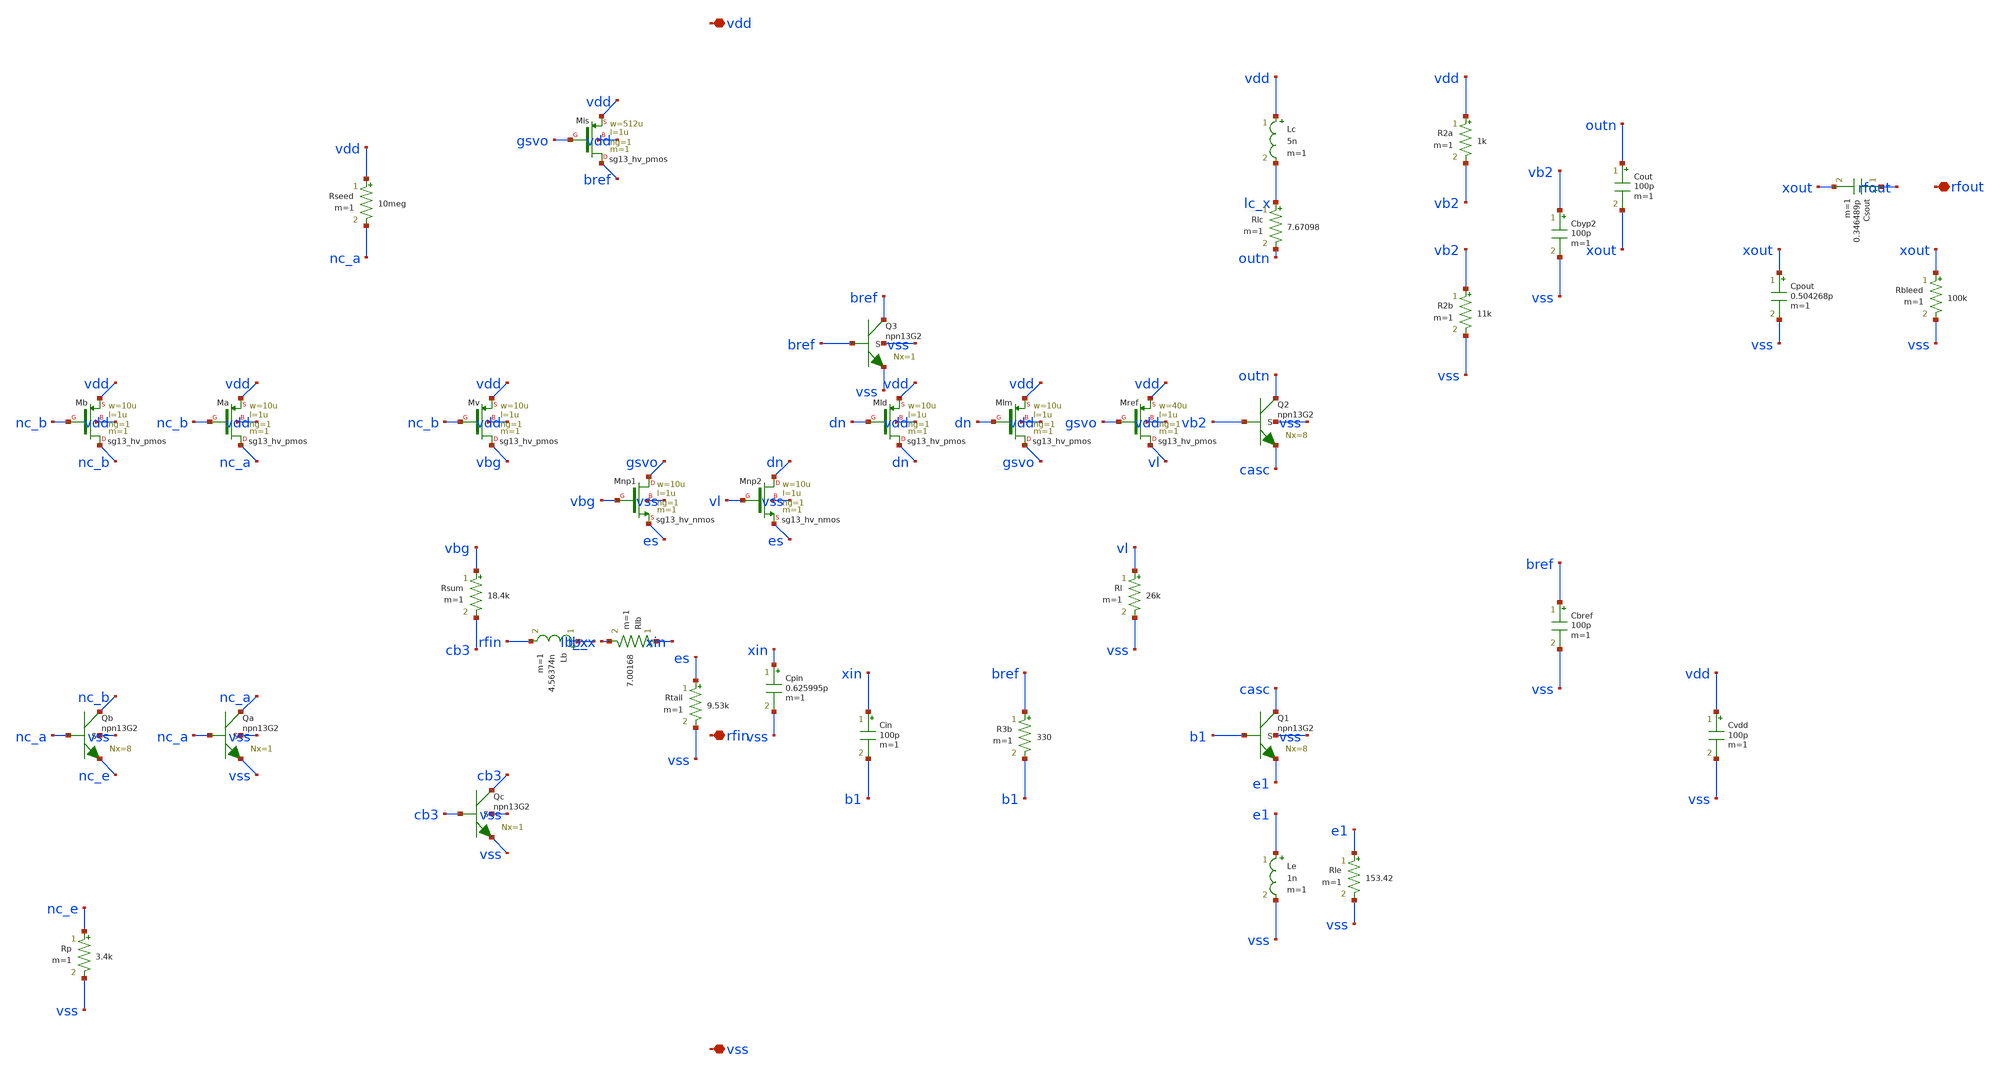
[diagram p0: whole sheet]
** sch_path: design/lna.sch
**.subckt lna vdd vss rfin rfout
*.iopin vdd
*.iopin vss
*.iopin rfin
*.iopin rfout
XQ2 outn vb2 casc vss npn13G2 Nx=8 mm_ok=1
XQ1 casc b1 e1 vss npn13G2 Nx=8 mm_ok=1
Le e1 vss 1n m=1
Rle e1 vss 153.42 m=1
Lc vdd lc_x 5n m=1
Rlc lc_x outn 7.67098 m=1
Cin xin b1 100p m=1
Cout outn xout 100p m=1
Lb lb_x rfin 4.56374n m=1
Rlb xin lb_x 7.00168 m=1
Cpin xin vss 0.625995p m=1
Cpout xout vss 0.504268p m=1
Csout rfout xout 0.346489p m=1
Rbleed xout vss 100k m=1
Cbyp2 vb2 vss 100p m=1
Cvdd vdd vss 100p m=1
R2a vdd vb2 1k m=1
R2b vb2 vss 11k m=1
XMb nc_b nc_b vdd vdd sg13_hv_pmos w=10u l=1u ng=1 m=1 mm_ok=1
XQb nc_b nc_a nc_e vss npn13G2 Nx=8 mm_ok=1
Rp nc_e vss 3.4k m=1
XMa nc_a nc_b vdd vdd sg13_hv_pmos w=10u l=1u ng=1 m=1 mm_ok=1
XQa nc_a nc_a vss vss npn13G2 Nx=1 mm_ok=1
Rseed vdd nc_a 10meg m=1
XMv vbg nc_b vdd vdd sg13_hv_pmos w=10u l=1u ng=1 m=1 mm_ok=1
Rsum vbg cb3 18.4k m=1
XQc cb3 cb3 vss vss npn13G2 Nx=1 mm_ok=1
XMnp1 gsvo vbg es vss sg13_hv_nmos w=10u l=1u ng=1 m=1 mm_ok=1
XMnp2 dn vl es vss sg13_hv_nmos w=10u l=1u ng=1 m=1 mm_ok=1
Rtail es vss 9.53k m=1
XMld dn dn vdd vdd sg13_hv_pmos w=10u l=1u ng=1 m=1 mm_ok=1
XMlm gsvo dn vdd vdd sg13_hv_pmos w=10u l=1u ng=1 m=1 mm_ok=1
XMref vl gsvo vdd vdd sg13_hv_pmos w=40u l=1u ng=1 m=1 mm_ok=1
Rl vl vss 26k m=1
XMis bref gsvo vdd vdd sg13_hv_pmos w=512u l=1u ng=1 m=1 mm_ok=1
R3b bref b1 330 m=1
XQ3 bref bref vss vss npn13G2 Nx=1 mm_ok=1
Cbref bref vss 100p m=1
**.ends
.end
